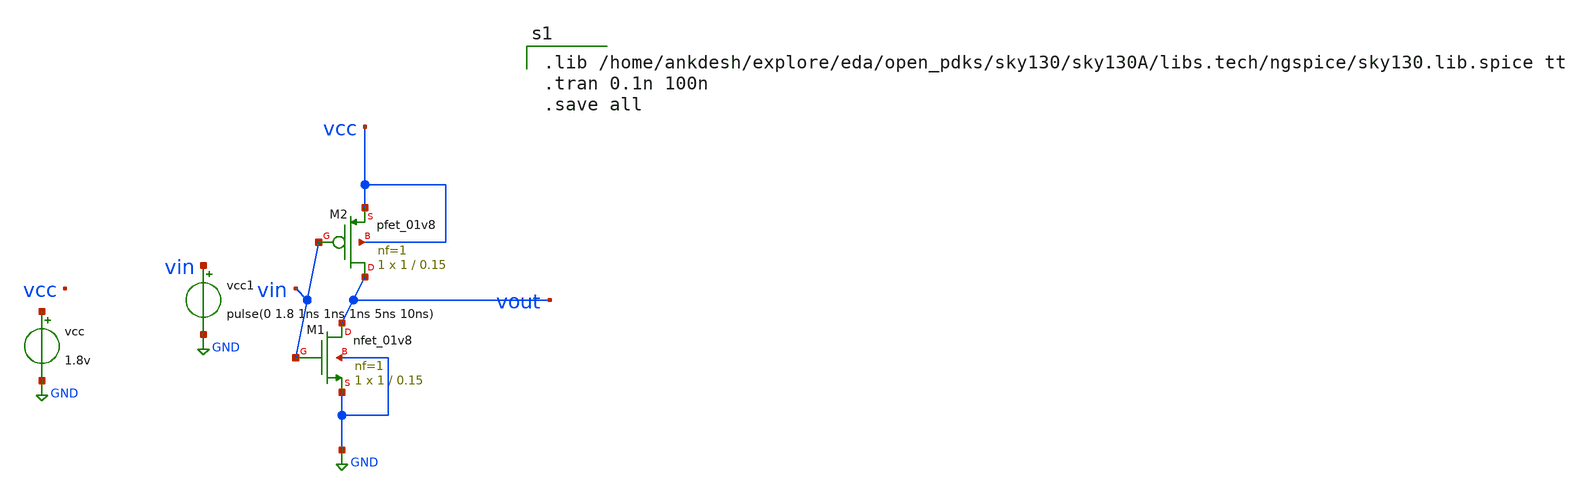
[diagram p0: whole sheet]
** sch_path: eda/xschem/asd_inv/asd_inv.sch
**.subckt asd_inv
vcc net1 GND 1.8v
vcc1 vin GND pulse(0 1.8 1ns 1ns 1ns 5ns 10ns)
XM1 vout vin GND GND sky130_fd_pr__nfet_01v8 L=0.15 W=1 nf=1 ad='int((nf+1)/2) * W/nf * 0.29' as='int((nf+2)/2) * W/nf * 0.29'
+ pd='2*int((nf+1)/2) * (W/nf + 0.29)' ps='2*int((nf+2)/2) * (W/nf + 0.29)' nrd='0.29 / W' nrs='0.29 / W'
+ sa=0 sb=0 sd=0 mult=1 m=1
XM2 vout vin vcc vcc sky130_fd_pr__pfet_01v8 L=0.15 W=1 nf=1 ad='int((nf+1)/2) * W/nf * 0.29' as='int((nf+2)/2) * W/nf * 0.29'
+ pd='2*int((nf+1)/2) * (W/nf + 0.29)' ps='2*int((nf+2)/2) * (W/nf + 0.29)' nrd='0.29 / W' nrs='0.29 / W'
+ sa=0 sb=0 sd=0 mult=1 m=1
**** begin user architecture code

.lib /home/ankdesh/explore/eda/open_pdks/sky130/sky130A/libs.tech/ngspice/sky130.lib.spice tt
.tran 0.1n 100n
.save all

**** end user architecture code
**.ends
.GLOBAL GND
.end
